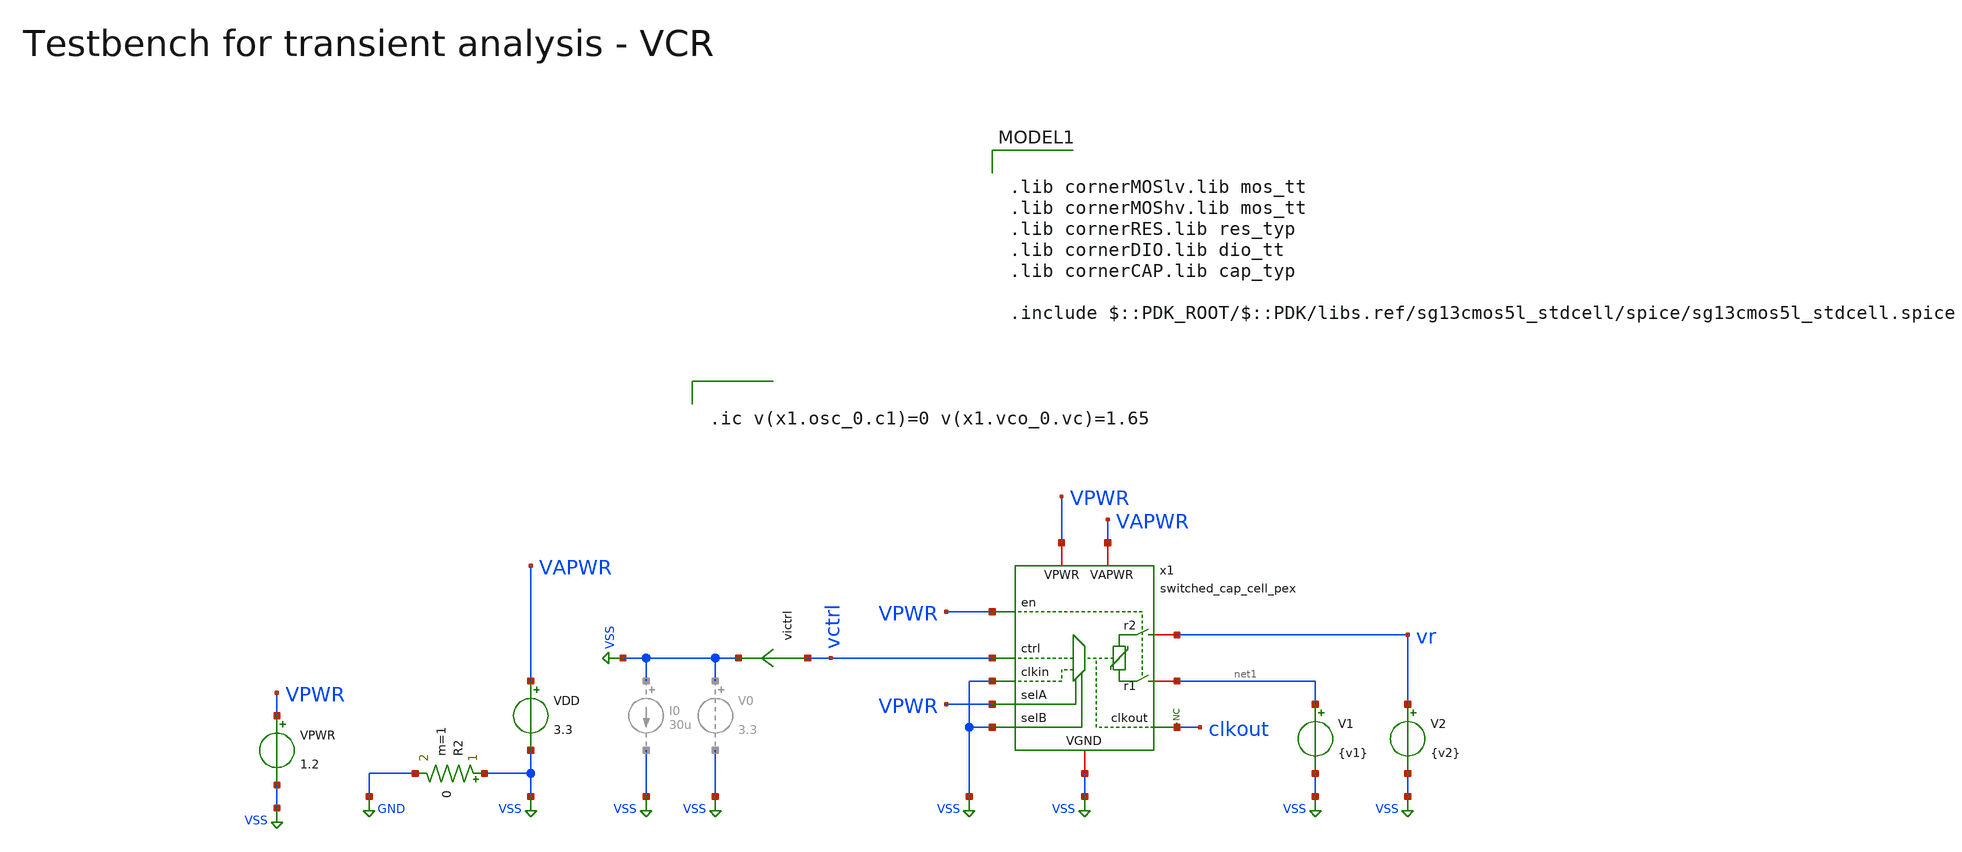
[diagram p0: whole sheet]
** sch_path: macros/heichips26_vcr/macros/switched_capacitor/testbenches/xschem/tb_switched_cap_pex_tran.sch
**.subckt tb_switched_cap_pex_tran
VDD VAPWR VSS 3.3
R2 VSS GND 0 m=1
V1 net1 VSS {v1}
V2 vr VSS {v2}
VPWR VPWR VSS 1.2
* noconn clkout
x1 vctrl VAPWR VSS vr net1 VSS VPWR VSS VPWR VPWR clkout switched_cap_cell_pex
victrl vctrl VSS 0
.save i(victrl)
**** begin user architecture code

.lib cornerMOSlv.lib mos_tt
.lib cornerMOShv.lib mos_tt
.lib cornerRES.lib res_typ
.lib cornerDIO.lib dio_tt
.lib cornerCAP.lib cap_typ

.include $::PDK_ROOT/$::PDK/libs.ref/sg13cmos5l_stdcell/spice/sg13cmos5l_stdcell.spice



.include ../../../netlist/pex/switched_cap_cell_magic_pex_1_manual_caps.spice

.param temp=27
.param vctrl  = 0.1
*.param f      = {2e6/vctrl}
.param f = 200Meg

* Derived timing parameters
.param period = {1/f}
.param ton    = {period/2}
.csparam tstop  = {10*period}
.csparam tstep  = {period/100}
.param ictrl  = {f*3.3e-12}
.param tr     = {period/1000}
.param tf     = {period/1000}

.param VDD = 3.3
.csparam VDD=VDD
.param vdm = 3.3
.param vcm = {VDD/2}
.param v1  = {vcm - vdm/2}
.param v2  = {vcm + vdm/2}

.options savecurrents klu method=gear reltol=1e-6 abstol=1e-12 gmin=1e-15
.probe alli
.control

save all
set appendwrite

tran {$&tstep} {$&tstop}
remzerovec

save all
set appendwrite

write @schname\.raw
set appendwrite

*let r_var = vr/i(r1)
meas tran period_sim TRIG i(V1) VAL=1m RISE=1 TARG i(V1) VAL=1m RISE=2
meas tran n_periods TRIG i(V1) VAL=1m RISE=1 TARG i(V1) VAL=1m RISE=LAST
meas tran i_avg AVG i(V1) FROM=0 TO=n_periods
meas tran v_avg AVG vr FROM=0 TO=n_periods
*meas tran r_avg AVG r_var

let npts = length(time) - 1
let i_mavg = integ(i(V1))[1, npts] / time[1, npts]
let v_mavg = integ(vr)[1, npts] / time[1, npts]
let r_mavg = v_mavg/i_mavg
let r_avg = v_avg/i_avg
let f_sim = 1/period_sim
let plot_y_lim = 1.2*r_avg

print period_sim f_sim r_avg

* Plotting
*plot vr v_avg v_mavg
plot i(V1) i_avg i_mavg
plot r_avg r_mavg ylimit 0 $&plot_y_lim
plot clkout
plot i(victrl) mean(i(victrl))
plot vctrl

* Write Data
unset appendwrite
set wr_vecnames
set wr_singlescale
wrdata ../plot_simulations/data/@schname\.txt v(vr) v(VDD) i(V1)

*quit
.endc




.ic v(x1.osc_0.c1)=0 v(x1.vco_0.vc)=1.65


**** end user architecture code
**.ends
.GLOBAL VSS
.GLOBAL GND
.end
